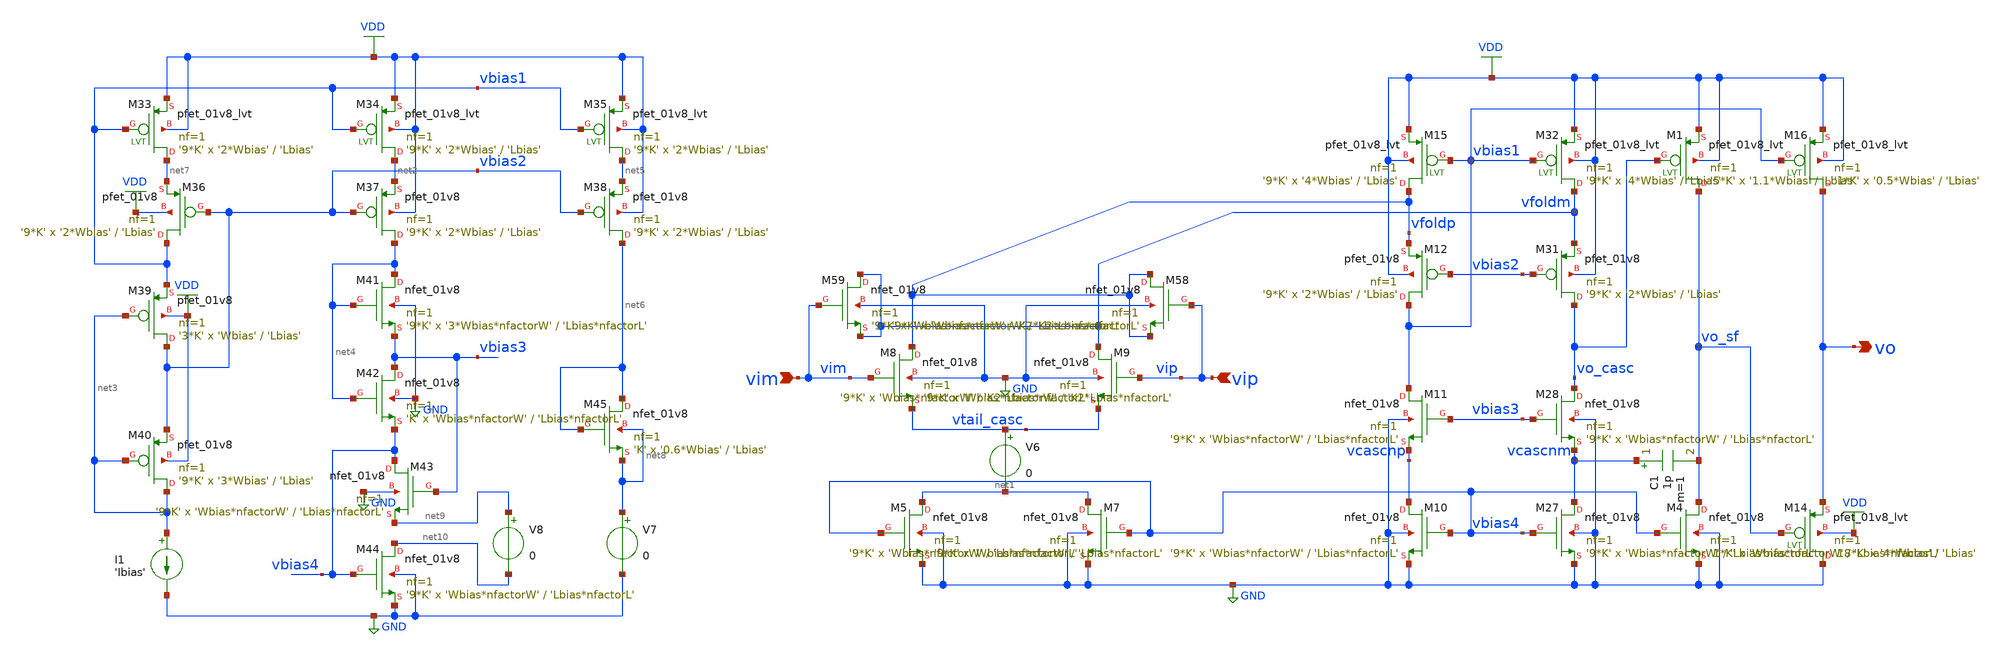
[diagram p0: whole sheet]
** sch_path: designs/se_fold_casc_opamp.sch
* Copyright 2020 Stefan Frederik Schippers
* Licensed under the Apache License, Version 2.0 (the "License");
* you may not use this file except in compliance with the License.
* You may obtain a copy of the License at
* https://www.apache.org/licenses/LICENSE-2.0
* Unless required by applicable law or agreed to in writing, software
* distributed under the License is distributed on an "AS IS" BASIS,
* WITHOUT WARRANTIES OR CONDITIONS OF ANY KIND, either express or implied.
* See the License for the specific language governing permissions and
* limitations under the License.
**.subckt se_fold_casc_opamp vim vip vo
*.ipin vim
*.ipin vip
*.opin vo
V6 vtail_casc net1 0
XM7 net1 vbias4 GND GND sky130_fd_pr__nfet_01v8 L='Lbias*nfactorL' W='Wbias*nfactorW' nf=1 ad='int((nf+1)/2) * W/nf * 0.29'
+ as='int((nf+2)/2) * W/nf * 0.29' pd='2*int((nf+1)/2) * (W/nf + 0.29)' ps='2*int((nf+2)/2) * (W/nf + 0.29)'
+ nrd='0.29 / W' nrs='0.29 / W' sa=0 sb=0 sd=0 mult='9*K' m='9*K'
XM10 vcascnp vbias4 GND GND sky130_fd_pr__nfet_01v8 L='Lbias*nfactorL' W='Wbias*nfactorW' nf=1 ad='int((nf+1)/2) * W/nf * 0.29'
+ as='int((nf+2)/2) * W/nf * 0.29' pd='2*int((nf+1)/2) * (W/nf + 0.29)' ps='2*int((nf+2)/2) * (W/nf + 0.29)'
+ nrd='0.29 / W' nrs='0.29 / W' sa=0 sb=0 sd=0 mult='9*K' m='9*K'
XM11 vbias1 vbias3 vcascnp GND sky130_fd_pr__nfet_01v8 L='Lbias*nfactorL' W='Wbias*nfactorW' nf=1 ad='int((nf+1)/2) * W/nf * 0.29'
+ as='int((nf+2)/2) * W/nf * 0.29' pd='2*int((nf+1)/2) * (W/nf + 0.29)' ps='2*int((nf+2)/2) * (W/nf + 0.29)'
+ nrd='0.29 / W' nrs='0.29 / W' sa=0 sb=0 sd=0 mult='9*K' m='9*K'
XM27 vcascnm vbias4 GND GND sky130_fd_pr__nfet_01v8 L='Lbias*nfactorL' W='Wbias*nfactorW' nf=1 ad='int((nf+1)/2) * W/nf * 0.29'
+ as='int((nf+2)/2) * W/nf * 0.29' pd='2*int((nf+1)/2) * (W/nf + 0.29)' ps='2*int((nf+2)/2) * (W/nf + 0.29)'
+ nrd='0.29 / W' nrs='0.29 / W' sa=0 sb=0 sd=0 mult='9*K' m='9*K'
XM28 vo_casc vbias3 vcascnm GND sky130_fd_pr__nfet_01v8 L='Lbias*nfactorL' W='Wbias*nfactorW' nf=1 ad='int((nf+1)/2) * W/nf * 0.29'
+ as='int((nf+2)/2) * W/nf * 0.29' pd='2*int((nf+1)/2) * (W/nf + 0.29)' ps='2*int((nf+2)/2) * (W/nf + 0.29)'
+ nrd='0.29 / W' nrs='0.29 / W' sa=0 sb=0 sd=0 mult='9*K' m='9*K'
XM36 vbias1 vbias2 net7 VDD sky130_fd_pr__pfet_01v8 L='Lbias' W='2*Wbias' nf=1 ad='int((nf+1)/2) * W/nf * 0.29'
+ as='int((nf+2)/2) * W/nf * 0.29' pd='2*int((nf+1)/2) * (W/nf + 0.29)' ps='2*int((nf+2)/2) * (W/nf + 0.29)'
+ nrd='0.29 / W' nrs='0.29 / W' sa=0 sb=0 sd=0 mult='9*K' m='9*K'
XM37 net4 vbias2 net2 VDD sky130_fd_pr__pfet_01v8 L='Lbias' W='2*Wbias' nf=1 ad='int((nf+1)/2) * W/nf * 0.29'
+ as='int((nf+2)/2) * W/nf * 0.29' pd='2*int((nf+1)/2) * (W/nf + 0.29)' ps='2*int((nf+2)/2) * (W/nf + 0.29)'
+ nrd='0.29 / W' nrs='0.29 / W' sa=0 sb=0 sd=0 mult='9*K' m='9*K'
XM38 net6 vbias2 net5 VDD sky130_fd_pr__pfet_01v8 L='Lbias' W='2*Wbias' nf=1 ad='int((nf+1)/2) * W/nf * 0.29'
+ as='int((nf+2)/2) * W/nf * 0.29' pd='2*int((nf+1)/2) * (W/nf + 0.29)' ps='2*int((nf+2)/2) * (W/nf + 0.29)'
+ nrd='0.29 / W' nrs='0.29 / W' sa=0 sb=0 sd=0 mult='9*K' m='9*K'
XM39 vbias2 net3 vbias1 VDD sky130_fd_pr__pfet_01v8 L='Lbias' W='Wbias' nf=1 ad='int((nf+1)/2) * W/nf * 0.29'
+ as='int((nf+2)/2) * W/nf * 0.29' pd='2*int((nf+1)/2) * (W/nf + 0.29)' ps='2*int((nf+2)/2) * (W/nf + 0.29)'
+ nrd='0.29 / W' nrs='0.29 / W' sa=0 sb=0 sd=0 mult='3*K' m='3*K'
XM40 net3 net3 vbias2 VDD sky130_fd_pr__pfet_01v8 L='Lbias' W='3*Wbias' nf=1 ad='int((nf+1)/2) * W/nf * 0.29'
+ as='int((nf+2)/2) * W/nf * 0.29' pd='2*int((nf+1)/2) * (W/nf + 0.29)' ps='2*int((nf+2)/2) * (W/nf + 0.29)'
+ nrd='0.29 / W' nrs='0.29 / W' sa=0 sb=0 sd=0 mult='9*K' m='9*K'
XM41 net4 net4 vbias3 GND sky130_fd_pr__nfet_01v8 L='Lbias*nfactorL' W='3*Wbias*nfactorW' nf=1 ad='int((nf+1)/2) * W/nf * 0.29'
+ as='int((nf+2)/2) * W/nf * 0.29' pd='2*int((nf+1)/2) * (W/nf + 0.29)' ps='2*int((nf+2)/2) * (W/nf + 0.29)'
+ nrd='0.29 / W' nrs='0.29 / W' sa=0 sb=0 sd=0 mult='9*K' m='9*K'
XM42 vbias3 net4 vbias4 GND sky130_fd_pr__nfet_01v8 L='Lbias*nfactorL' W='Wbias*nfactorW' nf=1 ad='int((nf+1)/2) * W/nf * 0.29'
+ as='int((nf+2)/2) * W/nf * 0.29' pd='2*int((nf+1)/2) * (W/nf + 0.29)' ps='2*int((nf+2)/2) * (W/nf + 0.29)'
+ nrd='0.29 / W' nrs='0.29 / W' sa=0 sb=0 sd=0 mult='K' m='K'
XM43 vbias4 vbias3 net9 GND sky130_fd_pr__nfet_01v8 L='Lbias*nfactorL' W='Wbias*nfactorW' nf=1 ad='int((nf+1)/2) * W/nf * 0.29'
+ as='int((nf+2)/2) * W/nf * 0.29' pd='2*int((nf+1)/2) * (W/nf + 0.29)' ps='2*int((nf+2)/2) * (W/nf + 0.29)'
+ nrd='0.29 / W' nrs='0.29 / W' sa=0 sb=0 sd=0 mult='9*K' m='9*K'
XM44 net10 vbias4 GND GND sky130_fd_pr__nfet_01v8 L='Lbias*nfactorL' W='Wbias*nfactorW' nf=1 ad='int((nf+1)/2) * W/nf * 0.29'
+ as='int((nf+2)/2) * W/nf * 0.29' pd='2*int((nf+1)/2) * (W/nf + 0.29)' ps='2*int((nf+2)/2) * (W/nf + 0.29)'
+ nrd='0.29 / W' nrs='0.29 / W' sa=0 sb=0 sd=0 mult='9*K' m='9*K'
XM45 net6 net6 net8 net8 sky130_fd_pr__nfet_01v8 L='Lbias' W='0.6*Wbias' nf=1 ad='int((nf+1)/2) * W/nf * 0.29'
+ as='int((nf+2)/2) * W/nf * 0.29' pd='2*int((nf+1)/2) * (W/nf + 0.29)' ps='2*int((nf+2)/2) * (W/nf + 0.29)'
+ nrd='0.29 / W' nrs='0.29 / W' sa=0 sb=0 sd=0 mult='K' m='K'
I1 net3 GND 'Ibias'
V7 net8 GND 0
V8 net9 net10 0
XM8 vfoldp vim vtail_casc GND sky130_fd_pr__nfet_01v8 L='K2*Lbias*nfactorL' W='Wbias*nfactorW' nf=1 ad='int((nf+1)/2) * W/nf * 0.29'
+ as='int((nf+2)/2) * W/nf * 0.29' pd='2*int((nf+1)/2) * (W/nf + 0.29)' ps='2*int((nf+2)/2) * (W/nf + 0.29)'
+ nrd='0.29 / W' nrs='0.29 / W' sa=0 sb=0 sd=0 mult='9*K' m='9*K'
XM12 vbias1 vbias2 vfoldp VDD sky130_fd_pr__pfet_01v8 L='Lbias' W='2*Wbias' nf=1 ad='int((nf+1)/2) * W/nf * 0.29'
+ as='int((nf+2)/2) * W/nf * 0.29' pd='2*int((nf+1)/2) * (W/nf + 0.29)' ps='2*int((nf+2)/2) * (W/nf + 0.29)'
+ nrd='0.29 / W' nrs='0.29 / W' sa=0 sb=0 sd=0 mult='9*K' m='9*K'
XM31 vo_casc vbias2 vfoldm VDD sky130_fd_pr__pfet_01v8 L='Lbias' W='2*Wbias' nf=1 ad='int((nf+1)/2) * W/nf * 0.29'
+ as='int((nf+2)/2) * W/nf * 0.29' pd='2*int((nf+1)/2) * (W/nf + 0.29)' ps='2*int((nf+2)/2) * (W/nf + 0.29)'
+ nrd='0.29 / W' nrs='0.29 / W' sa=0 sb=0 sd=0 mult='9*K' m='9*K'
XM15 vfoldp vbias1 VDD VDD sky130_fd_pr__pfet_01v8_lvt L='Lbias' W='4*Wbias' nf=1 ad='int((nf+1)/2) * W/nf * 0.29'
+ as='int((nf+2)/2) * W/nf * 0.29' pd='2*int((nf+1)/2) * (W/nf + 0.29)' ps='2*int((nf+2)/2) * (W/nf + 0.29)'
+ nrd='0.29 / W' nrs='0.29 / W' sa=0 sb=0 sd=0 mult='9*K' m='9*K'
XM32 vfoldm vbias1 VDD VDD sky130_fd_pr__pfet_01v8_lvt L='Lbias' W='4*Wbias' nf=1 ad='int((nf+1)/2) * W/nf * 0.29'
+ as='int((nf+2)/2) * W/nf * 0.29' pd='2*int((nf+1)/2) * (W/nf + 0.29)' ps='2*int((nf+2)/2) * (W/nf + 0.29)'
+ nrd='0.29 / W' nrs='0.29 / W' sa=0 sb=0 sd=0 mult='9*K' m='9*K'
XM33 net7 vbias1 VDD VDD sky130_fd_pr__pfet_01v8_lvt L='Lbias' W='2*Wbias' nf=1 ad='int((nf+1)/2) * W/nf * 0.29'
+ as='int((nf+2)/2) * W/nf * 0.29' pd='2*int((nf+1)/2) * (W/nf + 0.29)' ps='2*int((nf+2)/2) * (W/nf + 0.29)'
+ nrd='0.29 / W' nrs='0.29 / W' sa=0 sb=0 sd=0 mult='9*K' m='9*K'
XM34 net2 vbias1 VDD VDD sky130_fd_pr__pfet_01v8_lvt L='Lbias' W='2*Wbias' nf=1 ad='int((nf+1)/2) * W/nf * 0.29'
+ as='int((nf+2)/2) * W/nf * 0.29' pd='2*int((nf+1)/2) * (W/nf + 0.29)' ps='2*int((nf+2)/2) * (W/nf + 0.29)'
+ nrd='0.29 / W' nrs='0.29 / W' sa=0 sb=0 sd=0 mult='9*K' m='9*K'
XM35 net5 vbias1 VDD VDD sky130_fd_pr__pfet_01v8_lvt L='Lbias' W='2*Wbias' nf=1 ad='int((nf+1)/2) * W/nf * 0.29'
+ as='int((nf+2)/2) * W/nf * 0.29' pd='2*int((nf+1)/2) * (W/nf + 0.29)' ps='2*int((nf+2)/2) * (W/nf + 0.29)'
+ nrd='0.29 / W' nrs='0.29 / W' sa=0 sb=0 sd=0 mult='9*K' m='9*K'
XM5 net1 vbias4 GND GND sky130_fd_pr__nfet_01v8 L='Lbias*nfactorL' W='Wbias*nfactorW' nf=1 ad='int((nf+1)/2) * W/nf * 0.29'
+ as='int((nf+2)/2) * W/nf * 0.29' pd='2*int((nf+1)/2) * (W/nf + 0.29)' ps='2*int((nf+2)/2) * (W/nf + 0.29)'
+ nrd='0.29 / W' nrs='0.29 / W' sa=0 sb=0 sd=0 mult='9*K' m='9*K'
XM9 vfoldm vip vtail_casc GND sky130_fd_pr__nfet_01v8 L='K2*Lbias*nfactorL' W='Wbias*nfactorW' nf=1 ad='int((nf+1)/2) * W/nf * 0.29'
+ as='int((nf+2)/2) * W/nf * 0.29' pd='2*int((nf+1)/2) * (W/nf + 0.29)' ps='2*int((nf+2)/2) * (W/nf + 0.29)'
+ nrd='0.29 / W' nrs='0.29 / W' sa=0 sb=0 sd=0 mult='9*K' m='9*K'
XM58 vfoldp vip vfoldp GND sky130_fd_pr__nfet_01v8 L='K2*Lbias*nfactorL' W='Wbias*nfactorW' nf=1 ad='int((nf+1)/2) * W/nf * 0.29'
+ as='int((nf+2)/2) * W/nf * 0.29' pd='2*int((nf+1)/2) * (W/nf + 0.29)' ps='2*int((nf+2)/2) * (W/nf + 0.29)'
+ nrd='0.29 / W' nrs='0.29 / W' sa=0 sb=0 sd=0 mult='9*K' m='9*K'
XM59 vfoldm vim vfoldm GND sky130_fd_pr__nfet_01v8 L='K2*Lbias*nfactorL' W='Wbias*nfactorW' nf=1 ad='int((nf+1)/2) * W/nf * 0.29'
+ as='int((nf+2)/2) * W/nf * 0.29' pd='2*int((nf+1)/2) * (W/nf + 0.29)' ps='2*int((nf+2)/2) * (W/nf + 0.29)'
+ nrd='0.29 / W' nrs='0.29 / W' sa=0 sb=0 sd=0 mult='9*K' m='9*K'
XM4 vo_sf vbias4 GND GND sky130_fd_pr__nfet_01v8 L='Lbias*nfactorL' W='Wbias*nfactorW' nf=1 ad='int((nf+1)/2) * W/nf * 0.29'
+ as='int((nf+2)/2) * W/nf * 0.29' pd='2*int((nf+1)/2) * (W/nf + 0.29)' ps='2*int((nf+2)/2) * (W/nf + 0.29)'
+ nrd='0.29 / W' nrs='0.29 / W' sa=0 sb=0 sd=0 mult='1*K' m='1*K'
XM14 GND vo_sf vo VDD sky130_fd_pr__pfet_01v8_lvt L='Lbias' W='4*Wbias' nf=1 ad='int((nf+1)/2) * W/nf * 0.29'
+ as='int((nf+2)/2) * W/nf * 0.29' pd='2*int((nf+1)/2) * (W/nf + 0.29)' ps='2*int((nf+2)/2) * (W/nf + 0.29)'
+ nrd='0.29 / W' nrs='0.29 / W' sa=0 sb=0 sd=0 mult='18*K' m='18*K'
XM16 vo vbias1 VDD VDD sky130_fd_pr__pfet_01v8_lvt L='Lbias' W='0.5*Wbias' nf=1 ad='int((nf+1)/2) * W/nf * 0.29'
+ as='int((nf+2)/2) * W/nf * 0.29' pd='2*int((nf+1)/2) * (W/nf + 0.29)' ps='2*int((nf+2)/2) * (W/nf + 0.29)'
+ nrd='0.29 / W' nrs='0.29 / W' sa=0 sb=0 sd=0 mult='1*K' m='1*K'
C1 vcascnm vo_sf 1p m=1
XM1 vo_sf vo_casc VDD VDD sky130_fd_pr__pfet_01v8_lvt L='Lbias' W='1.1*Wbias' nf=1 ad='int((nf+1)/2) * W/nf * 0.29'
+ as='int((nf+2)/2) * W/nf * 0.29' pd='2*int((nf+1)/2) * (W/nf + 0.29)' ps='2*int((nf+2)/2) * (W/nf + 0.29)'
+ nrd='0.29 / W' nrs='0.29 / W' sa=0 sb=0 sd=0 mult='5*K' m='5*K'
**** begin user architecture code

.include $::SKYWATER_MODELS/cells/nfet_01v8/sky130_fd_pr__nfet_01v8__tt.corner.spice
.include $::SKYWATER_MODELS/cells/nfet_01v8_lvt/sky130_fd_pr__nfet_01v8_lvt__tt.corner.spice
.include $::SKYWATER_MODELS/cells/pfet_01v8/sky130_fd_pr__pfet_01v8__tt.corner.spice
.include $::SKYWATER_MODELS/cells/nfet_03v3_nvt/sky130_fd_pr__nfet_03v3_nvt__tt.corner.spice
.include $::SKYWATER_MODELS/cells/nfet_05v0_nvt/sky130_fd_pr__nfet_05v0_nvt__tt.corner.spice
.include $::SKYWATER_MODELS/cells/esd_nfet_01v8/sky130_fd_pr__esd_nfet_01v8__tt.corner.spice
.include $::SKYWATER_MODELS/cells/pfet_01v8_lvt/sky130_fd_pr__pfet_01v8_lvt__tt.corner.spice
.include $::SKYWATER_MODELS/cells/pfet_01v8_hvt/sky130_fd_pr__pfet_01v8_hvt__tt.corner.spice
.include $::SKYWATER_MODELS/cells/esd_pfet_g5v0d10v5/sky130_fd_pr__esd_pfet_g5v0d10v5__tt.corner.spice
.include $::SKYWATER_MODELS/cells/pfet_g5v0d10v5/sky130_fd_pr__pfet_g5v0d10v5__tt.corner.spice
.include $::SKYWATER_MODELS/cells/pfet_g5v0d16v0/sky130_fd_pr__pfet_g5v0d16v0__tt.corner.spice
.include $::SKYWATER_MODELS/cells/nfet_g5v0d10v5/sky130_fd_pr__nfet_g5v0d10v5__tt.corner.spice
.include $::SKYWATER_MODELS/cells/nfet_g5v0d16v0/sky130_fd_pr__nfet_g5v0d16v0__tt_discrete.corner.spice
.include $::SKYWATER_MODELS/cells/esd_nfet_g5v0d10v5/sky130_fd_pr__esd_nfet_g5v0d10v5__tt.corner.spice
.include $::SKYWATER_MODELS/models/corners/tt/nonfet.spice
* Mismatch parameters
.include $::SKYWATER_MODELS/cells/nfet_01v8/sky130_fd_pr__nfet_01v8__mismatch.corner.spice
.include $::SKYWATER_MODELS/cells/pfet_01v8/sky130_fd_pr__pfet_01v8__mismatch.corner.spice
.include $::SKYWATER_MODELS/cells/nfet_01v8_lvt/sky130_fd_pr__nfet_01v8_lvt__mismatch.corner.spice
.include $::SKYWATER_MODELS/cells/pfet_01v8_lvt/sky130_fd_pr__pfet_01v8_lvt__mismatch.corner.spice
.include $::SKYWATER_MODELS/cells/pfet_01v8_hvt/sky130_fd_pr__pfet_01v8_hvt__mismatch.corner.spice
.include $::SKYWATER_MODELS/cells/nfet_g5v0d10v5/sky130_fd_pr__nfet_g5v0d10v5__mismatch.corner.spice
.include $::SKYWATER_MODELS/cells/pfet_g5v0d10v5/sky130_fd_pr__pfet_g5v0d10v5__mismatch.corner.spice
.include $::SKYWATER_MODELS/cells/nfet_05v0_nvt/sky130_fd_pr__nfet_05v0_nvt__mismatch.corner.spice
.include $::SKYWATER_MODELS/cells/nfet_03v3_nvt/sky130_fd_pr__nfet_03v3_nvt__mismatch.corner.spice
* Resistor$::SKYWATER_MODELS/Capacitor
.include $::SKYWATER_MODELS/models/r+c/res_typical__cap_typical.spice
.include $::SKYWATER_MODELS/models/r+c/res_typical__cap_typical__lin.spice
* Special cells
.include $::SKYWATER_MODELS/models/corners/tt/specialized_cells.spice
* All models
.include $::SKYWATER_MODELS/models/all.spice
* Corner
.include $::SKYWATER_MODELS/models/corners/tt/rf.spice

**** end user architecture code
**.ends
.GLOBAL GND
.GLOBAL VDD
**** begin user architecture code

.include se_fold_casc_opamp_commands.spice

**** end user architecture code
.end
